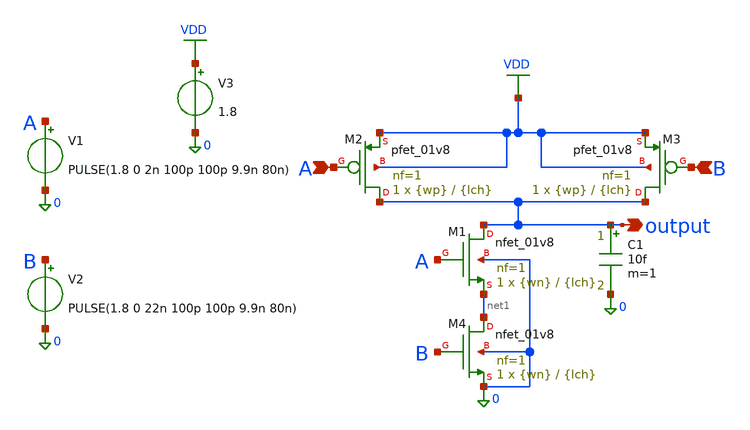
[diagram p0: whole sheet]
** sch_path: testWLnand2.sch
**.subckt testWLnand2 output A B
*.opin output
*.ipin A
*.ipin B
XM1 output A net1 0 sky130_fd_pr__nfet_01v8 L={lch} W={wn} nf=1 ad='int((1 + 1)/2) * {wn} / 1 * 0.29'
+ as='int((1 + 2)/2) * {wn} / 1 * 0.29' pd='2*int((1 + 1)/2) * ({wn} / 1 + 0.29)' ps='2*int((1 + 2)/2) * ({wn} / 1 + 0.29)'
+ nrd='0.29 / {wn} ' nrs='0.29 / {wn} ' sa=0 sb=0 sd=0 mult=1 m=1
XM2 output A VDD VDD sky130_fd_pr__pfet_01v8 L={lch} W={wp} nf=1 ad='int((1 + 1)/2) * {wp} / 1 * 0.29'
+ as='int((1 + 2)/2) * {wp} / 1 * 0.29' pd='2*int((1 + 1)/2) * ({wp} / 1 + 0.29)' ps='2*int((1 + 2)/2) * ({wp} / 1 + 0.29)'
+ nrd='0.29 / {wp} ' nrs='0.29 / {wp} ' sa=0 sb=0 sd=0 mult=1 m=1
XM3 output B VDD VDD sky130_fd_pr__pfet_01v8 L={lch} W={wp} nf=1 ad='int((1 + 1)/2) * {wp} / 1 * 0.29'
+ as='int((1 + 2)/2) * {wp} / 1 * 0.29' pd='2*int((1 + 1)/2) * ({wp} / 1 + 0.29)' ps='2*int((1 + 2)/2) * ({wp} / 1 + 0.29)'
+ nrd='0.29 / {wp} ' nrs='0.29 / {wp} ' sa=0 sb=0 sd=0 mult=1 m=1
XM4 net1 B 0 0 sky130_fd_pr__nfet_01v8 L={lch} W={wn} nf=1 ad='int((1 + 1)/2) * {wn} / 1 * 0.29' as='int((1 + 2)/2) * {wn} / 1 * 0.29'
+ pd='2*int((1 + 1)/2) * ({wn} / 1 + 0.29)' ps='2*int((1 + 2)/2) * ({wn} / 1 + 0.29)' nrd='0.29 / {wn} '
+ nrs='0.29 / {wn} ' sa=0 sb=0 sd=0 mult=1 m=1
V1 A 0 PULSE(1.8 0 2n 100p 100p 9.9n 80n)
V2 B 0 PULSE(1.8 0 22n 100p 100p 9.9n 80n)
V3 VDD 0 1.8
C1 output 0 10f m=1
**** begin user architecture code
.lib /foss/pdks/sky130A/libs.tech/ngspice/sky130.lib.spice tt
.temp 27
.param lch=0.15
.param wn=3.0
.param wp=6.0
.control
echo L_um "|" Wn_um "|" Wp_um "|" tplh_A_ps "|" tphl_A_ps "|" tplh_B_ps "|" tphl_B_ps "|" tpd_A_ps
+ "|" tpd_B_ps "|" Pavg_uW "|" Cin_A_fF "|" Cin_B_fF > /foss/designs/nand_L_results.txt
foreach l 0.15 0.18 0.20 0.25 0.30 0.40
    alterparam lch=$l
    reset
    tran 5p 80n

    meas tran tplh_a TRIG v(a) VAL=0.9 FALL=1 TARG v(output) VAL=0.9 RISE=1
    meas tran tphl_a TRIG v(a) VAL=0.9 RISE=1 TARG v(output) VAL=0.9 FALL=1
    meas tran tplh_b TRIG v(b) VAL=0.9 FALL=1 TARG v(output) VAL=0.9 RISE=2
    meas tran tphl_b TRIG v(b) VAL=0.9 RISE=1 TARG v(output) VAL=0.9 FALL=2

    let tplh_a_ps = tplh_a*1e12
    let tphl_a_ps = tphl_a*1e12
    let tplh_b_ps = tplh_b*1e12
    let tphl_b_ps = tphl_b*1e12
    let tpd_a_ps = (tplh_a + tphl_a)/2*1e12
    let tpd_b_ps = (tplh_b + tphl_b)/2*1e12

    meas tran iavg AVG i(v3) FROM=0 TO=80n
    let pavg_uw = -1.8*iavg*1e6
    meas tran qa INTEG i(v1) FROM=12n TO=14n
    meas tran qb INTEG i(v2) FROM=32n TO=34n

    let cin_a_ff = -qa/1.8*1e15
    let cin_b_ff = -qb/1.8*1e15

    echo $l "|" 3.0 "|" 6.0 "|" $&tplh_a_ps "|" $&tphl_a_ps "|" $&tplh_b_ps "|" $&tphl_b_ps "|"
+ $&tpd_a_ps "|" $&tpd_b_ps "|" $&pavg_uw "|" $&cin_a_ff "|" $&cin_b_ff >> /foss/designs/nand_L_results.txt

end

.endc
**** end user architecture code
**.ends
.GLOBAL VDD
.end
